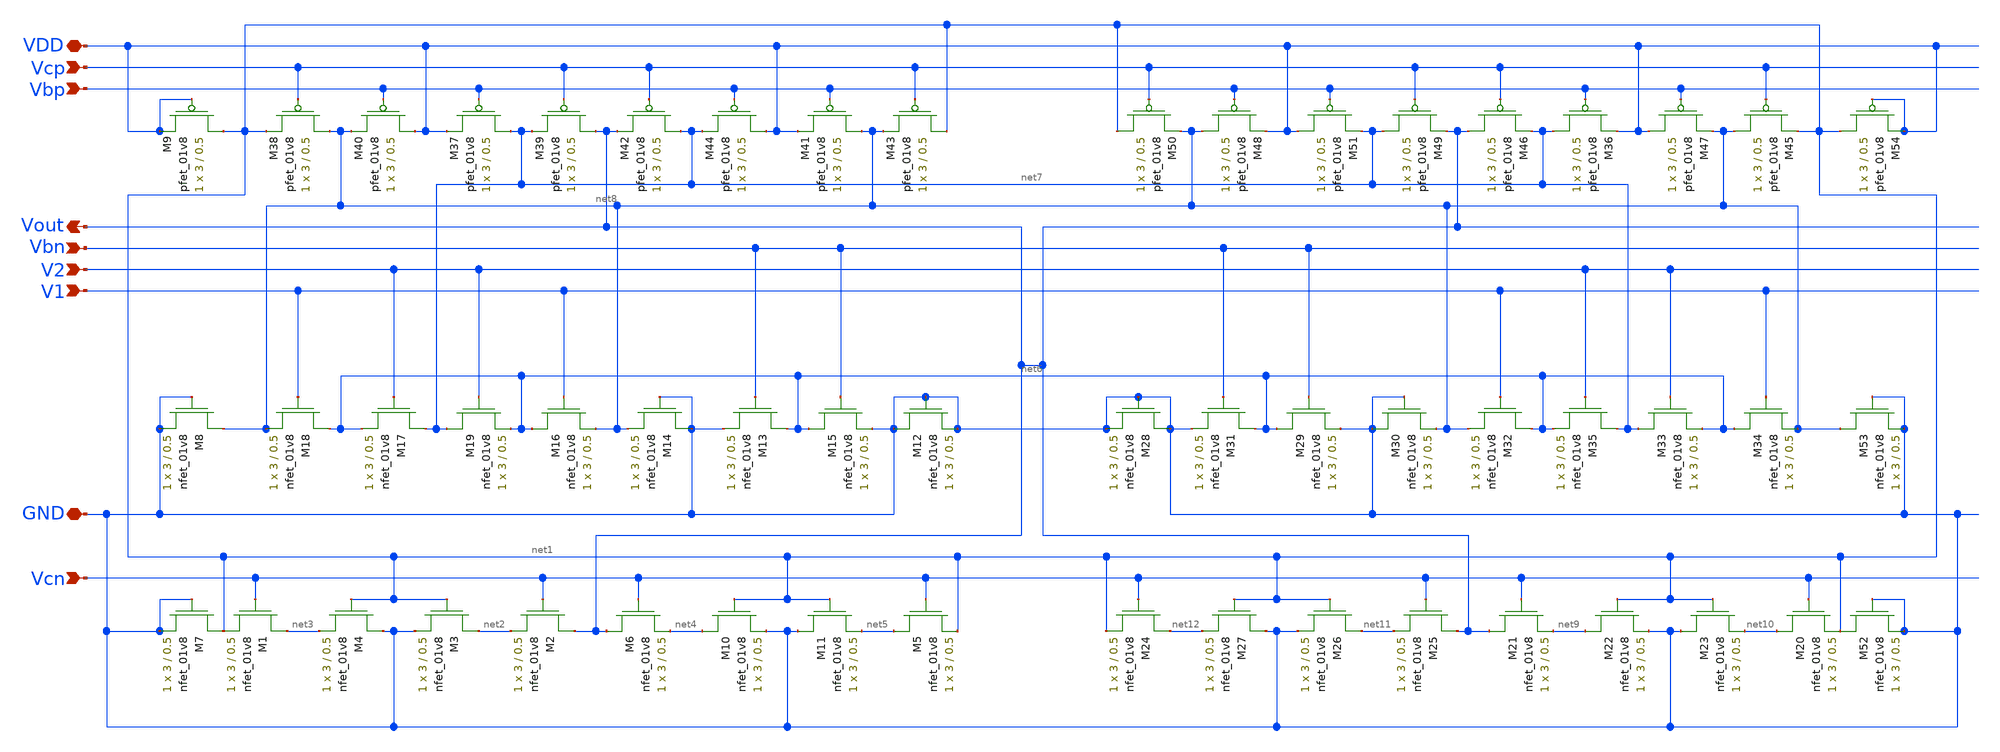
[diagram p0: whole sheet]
** sch_path: Miniproject3/layout&schematics/opamp.sch
**.subckt opamp Vcn Vout GND V1 V2 Vbn Vbp VDD Vcp
*.ipin Vcn
*.opin Vout
*.iopin GND
*.ipin V1
*.ipin V2
*.ipin Vbn
*.ipin Vbp
*.iopin VDD
*.ipin Vcp
XM1 net3 Vcn net1 GND sky130_fd_pr__nfet_01v8 L=0.5 W=3 nf=1 ad='int((nf+1)/2) * W/nf * 0.29' as='int((nf+2)/2) * W/nf * 0.29'
+ pd='2*int((nf+1)/2) * (W/nf + 0.29)' ps='2*int((nf+2)/2) * (W/nf + 0.29)' nrd='0.29 / W' nrs='0.29 / W'
+ sa=0 sb=0 sd=0 mult=1 m=1
XM2 Vout Vcn net2 GND sky130_fd_pr__nfet_01v8 L=0.5 W=3 nf=1 ad='int((nf+1)/2) * W/nf * 0.29' as='int((nf+2)/2) * W/nf * 0.29'
+ pd='2*int((nf+1)/2) * (W/nf + 0.29)' ps='2*int((nf+2)/2) * (W/nf + 0.29)' nrd='0.29 / W' nrs='0.29 / W'
+ sa=0 sb=0 sd=0 mult=1 m=1
XM3 net2 net1 GND GND sky130_fd_pr__nfet_01v8 L=0.5 W=3 nf=1 ad='int((nf+1)/2) * W/nf * 0.29' as='int((nf+2)/2) * W/nf * 0.29'
+ pd='2*int((nf+1)/2) * (W/nf + 0.29)' ps='2*int((nf+2)/2) * (W/nf + 0.29)' nrd='0.29 / W' nrs='0.29 / W'
+ sa=0 sb=0 sd=0 mult=1 m=1
XM4 GND net1 net3 GND sky130_fd_pr__nfet_01v8 L=0.5 W=3 nf=1 ad='int((nf+1)/2) * W/nf * 0.29' as='int((nf+2)/2) * W/nf * 0.29'
+ pd='2*int((nf+1)/2) * (W/nf + 0.29)' ps='2*int((nf+2)/2) * (W/nf + 0.29)' nrd='0.29 / W' nrs='0.29 / W'
+ sa=0 sb=0 sd=0 mult=1 m=1
XM5 net5 Vcn net1 GND sky130_fd_pr__nfet_01v8 L=0.5 W=3 nf=1 ad='int((nf+1)/2) * W/nf * 0.29' as='int((nf+2)/2) * W/nf * 0.29'
+ pd='2*int((nf+1)/2) * (W/nf + 0.29)' ps='2*int((nf+2)/2) * (W/nf + 0.29)' nrd='0.29 / W' nrs='0.29 / W'
+ sa=0 sb=0 sd=0 mult=1 m=1
XM6 Vout Vcn net4 GND sky130_fd_pr__nfet_01v8 L=0.5 W=3 nf=1 ad='int((nf+1)/2) * W/nf * 0.29' as='int((nf+2)/2) * W/nf * 0.29'
+ pd='2*int((nf+1)/2) * (W/nf + 0.29)' ps='2*int((nf+2)/2) * (W/nf + 0.29)' nrd='0.29 / W' nrs='0.29 / W'
+ sa=0 sb=0 sd=0 mult=1 m=1
XM10 net4 net1 GND GND sky130_fd_pr__nfet_01v8 L=0.5 W=3 nf=1 ad='int((nf+1)/2) * W/nf * 0.29' as='int((nf+2)/2) * W/nf * 0.29'
+ pd='2*int((nf+1)/2) * (W/nf + 0.29)' ps='2*int((nf+2)/2) * (W/nf + 0.29)' nrd='0.29 / W' nrs='0.29 / W'
+ sa=0 sb=0 sd=0 mult=1 m=1
XM11 GND net1 net5 GND sky130_fd_pr__nfet_01v8 L=0.5 W=3 nf=1 ad='int((nf+1)/2) * W/nf * 0.29' as='int((nf+2)/2) * W/nf * 0.29'
+ pd='2*int((nf+1)/2) * (W/nf + 0.29)' ps='2*int((nf+2)/2) * (W/nf + 0.29)' nrd='0.29 / W' nrs='0.29 / W'
+ sa=0 sb=0 sd=0 mult=1 m=1
XM12 GND GND GND GND sky130_fd_pr__nfet_01v8 L=0.5 W=3 nf=1 ad='int((nf+1)/2) * W/nf * 0.29' as='int((nf+2)/2) * W/nf * 0.29'
+ pd='2*int((nf+1)/2) * (W/nf + 0.29)' ps='2*int((nf+2)/2) * (W/nf + 0.29)' nrd='0.29 / W' nrs='0.29 / W'
+ sa=0 sb=0 sd=0 mult=1 m=1
XM13 net6 Vbn GND GND sky130_fd_pr__nfet_01v8 L=0.5 W=3 nf=1 ad='int((nf+1)/2) * W/nf * 0.29' as='int((nf+2)/2) * W/nf * 0.29'
+ pd='2*int((nf+1)/2) * (W/nf + 0.29)' ps='2*int((nf+2)/2) * (W/nf + 0.29)' nrd='0.29 / W' nrs='0.29 / W'
+ sa=0 sb=0 sd=0 mult=1 m=1
XM14 GND GND net8 GND sky130_fd_pr__nfet_01v8 L=0.5 W=3 nf=1 ad='int((nf+1)/2) * W/nf * 0.29' as='int((nf+2)/2) * W/nf * 0.29'
+ pd='2*int((nf+1)/2) * (W/nf + 0.29)' ps='2*int((nf+2)/2) * (W/nf + 0.29)' nrd='0.29 / W' nrs='0.29 / W'
+ sa=0 sb=0 sd=0 mult=1 m=1
XM15 net6 Vbn GND GND sky130_fd_pr__nfet_01v8 L=0.5 W=3 nf=1 ad='int((nf+1)/2) * W/nf * 0.29' as='int((nf+2)/2) * W/nf * 0.29'
+ pd='2*int((nf+1)/2) * (W/nf + 0.29)' ps='2*int((nf+2)/2) * (W/nf + 0.29)' nrd='0.29 / W' nrs='0.29 / W'
+ sa=0 sb=0 sd=0 mult=1 m=1
XM16 net6 V1 net8 GND sky130_fd_pr__nfet_01v8 L=0.5 W=3 nf=1 ad='int((nf+1)/2) * W/nf * 0.29' as='int((nf+2)/2) * W/nf * 0.29'
+ pd='2*int((nf+1)/2) * (W/nf + 0.29)' ps='2*int((nf+2)/2) * (W/nf + 0.29)' nrd='0.29 / W' nrs='0.29 / W'
+ sa=0 sb=0 sd=0 mult=1 m=1
XM17 net7 V2 net6 GND sky130_fd_pr__nfet_01v8 L=0.5 W=3 nf=1 ad='int((nf+1)/2) * W/nf * 0.29' as='int((nf+2)/2) * W/nf * 0.29'
+ pd='2*int((nf+1)/2) * (W/nf + 0.29)' ps='2*int((nf+2)/2) * (W/nf + 0.29)' nrd='0.29 / W' nrs='0.29 / W'
+ sa=0 sb=0 sd=0 mult=1 m=1
XM18 net6 V1 net8 GND sky130_fd_pr__nfet_01v8 L=0.5 W=3 nf=1 ad='int((nf+1)/2) * W/nf * 0.29' as='int((nf+2)/2) * W/nf * 0.29'
+ pd='2*int((nf+1)/2) * (W/nf + 0.29)' ps='2*int((nf+2)/2) * (W/nf + 0.29)' nrd='0.29 / W' nrs='0.29 / W'
+ sa=0 sb=0 sd=0 mult=1 m=1
XM19 net7 V2 net6 GND sky130_fd_pr__nfet_01v8 L=0.5 W=3 nf=1 ad='int((nf+1)/2) * W/nf * 0.29' as='int((nf+2)/2) * W/nf * 0.29'
+ pd='2*int((nf+1)/2) * (W/nf + 0.29)' ps='2*int((nf+2)/2) * (W/nf + 0.29)' nrd='0.29 / W' nrs='0.29 / W'
+ sa=0 sb=0 sd=0 mult=1 m=1
XM37 net7 Vbp VDD VDD sky130_fd_pr__pfet_01v8 L=0.5 W=3 nf=1 ad='int((nf+1)/2) * W/nf * 0.29' as='int((nf+2)/2) * W/nf * 0.29'
+ pd='2*int((nf+1)/2) * (W/nf + 0.29)' ps='2*int((nf+2)/2) * (W/nf + 0.29)' nrd='0.29 / W' nrs='0.29 / W'
+ sa=0 sb=0 sd=0 mult=1 m=1
XM38 net8 Vcp net1 VDD sky130_fd_pr__pfet_01v8 L=0.5 W=3 nf=1 ad='int((nf+1)/2) * W/nf * 0.29' as='int((nf+2)/2) * W/nf * 0.29'
+ pd='2*int((nf+1)/2) * (W/nf + 0.29)' ps='2*int((nf+2)/2) * (W/nf + 0.29)' nrd='0.29 / W' nrs='0.29 / W'
+ sa=0 sb=0 sd=0 mult=1 m=1
XM39 Vout Vcp net7 VDD sky130_fd_pr__pfet_01v8 L=0.5 W=3 nf=1 ad='int((nf+1)/2) * W/nf * 0.29' as='int((nf+2)/2) * W/nf * 0.29'
+ pd='2*int((nf+1)/2) * (W/nf + 0.29)' ps='2*int((nf+2)/2) * (W/nf + 0.29)' nrd='0.29 / W' nrs='0.29 / W'
+ sa=0 sb=0 sd=0 mult=1 m=1
XM40 VDD Vbp net8 VDD sky130_fd_pr__pfet_01v8 L=0.5 W=3 nf=1 ad='int((nf+1)/2) * W/nf * 0.29' as='int((nf+2)/2) * W/nf * 0.29'
+ pd='2*int((nf+1)/2) * (W/nf + 0.29)' ps='2*int((nf+2)/2) * (W/nf + 0.29)' nrd='0.29 / W' nrs='0.29 / W'
+ sa=0 sb=0 sd=0 mult=1 m=1
XM41 net8 Vbp VDD VDD sky130_fd_pr__pfet_01v8 L=0.5 W=3 nf=1 ad='int((nf+1)/2) * W/nf * 0.29' as='int((nf+2)/2) * W/nf * 0.29'
+ pd='2*int((nf+1)/2) * (W/nf + 0.29)' ps='2*int((nf+2)/2) * (W/nf + 0.29)' nrd='0.29 / W' nrs='0.29 / W'
+ sa=0 sb=0 sd=0 mult=1 m=1
XM42 net7 Vcp Vout VDD sky130_fd_pr__pfet_01v8 L=0.5 W=3 nf=1 ad='int((nf+1)/2) * W/nf * 0.29' as='int((nf+2)/2) * W/nf * 0.29'
+ pd='2*int((nf+1)/2) * (W/nf + 0.29)' ps='2*int((nf+2)/2) * (W/nf + 0.29)' nrd='0.29 / W' nrs='0.29 / W'
+ sa=0 sb=0 sd=0 mult=1 m=1
XM43 net1 Vcp net8 VDD sky130_fd_pr__pfet_01v8 L=0.5 W=3 nf=1 ad='int((nf+1)/2) * W/nf * 0.29' as='int((nf+2)/2) * W/nf * 0.29'
+ pd='2*int((nf+1)/2) * (W/nf + 0.29)' ps='2*int((nf+2)/2) * (W/nf + 0.29)' nrd='0.29 / W' nrs='0.29 / W'
+ sa=0 sb=0 sd=0 mult=1 m=1
XM44 VDD Vbp net7 VDD sky130_fd_pr__pfet_01v8 L=0.5 W=3 nf=1 ad='int((nf+1)/2) * W/nf * 0.29' as='int((nf+2)/2) * W/nf * 0.29'
+ pd='2*int((nf+1)/2) * (W/nf + 0.29)' ps='2*int((nf+2)/2) * (W/nf + 0.29)' nrd='0.29 / W' nrs='0.29 / W'
+ sa=0 sb=0 sd=0 mult=1 m=1
XM7 net1 GND GND GND sky130_fd_pr__nfet_01v8 L=0.5 W=3 nf=1 ad='int((nf+1)/2) * W/nf * 0.29' as='int((nf+2)/2) * W/nf * 0.29'
+ pd='2*int((nf+1)/2) * (W/nf + 0.29)' ps='2*int((nf+2)/2) * (W/nf + 0.29)' nrd='0.29 / W' nrs='0.29 / W'
+ sa=0 sb=0 sd=0 mult=1 m=1
XM8 net8 GND GND GND sky130_fd_pr__nfet_01v8 L=0.5 W=3 nf=1 ad='int((nf+1)/2) * W/nf * 0.29' as='int((nf+2)/2) * W/nf * 0.29'
+ pd='2*int((nf+1)/2) * (W/nf + 0.29)' ps='2*int((nf+2)/2) * (W/nf + 0.29)' nrd='0.29 / W' nrs='0.29 / W'
+ sa=0 sb=0 sd=0 mult=1 m=1
XM9 net1 VDD VDD VDD sky130_fd_pr__pfet_01v8 L=0.5 W=3 nf=1 ad='int((nf+1)/2) * W/nf * 0.29' as='int((nf+2)/2) * W/nf * 0.29'
+ pd='2*int((nf+1)/2) * (W/nf + 0.29)' ps='2*int((nf+2)/2) * (W/nf + 0.29)' nrd='0.29 / W' nrs='0.29 / W'
+ sa=0 sb=0 sd=0 mult=1 m=1
XM20 net10 Vcn net1 GND sky130_fd_pr__nfet_01v8 L=0.5 W=3 nf=1 ad='int((nf+1)/2) * W/nf * 0.29' as='int((nf+2)/2) * W/nf * 0.29'
+ pd='2*int((nf+1)/2) * (W/nf + 0.29)' ps='2*int((nf+2)/2) * (W/nf + 0.29)' nrd='0.29 / W' nrs='0.29 / W'
+ sa=0 sb=0 sd=0 mult=1 m=1
XM21 Vout Vcn net9 GND sky130_fd_pr__nfet_01v8 L=0.5 W=3 nf=1 ad='int((nf+1)/2) * W/nf * 0.29' as='int((nf+2)/2) * W/nf * 0.29'
+ pd='2*int((nf+1)/2) * (W/nf + 0.29)' ps='2*int((nf+2)/2) * (W/nf + 0.29)' nrd='0.29 / W' nrs='0.29 / W'
+ sa=0 sb=0 sd=0 mult=1 m=1
XM22 net9 net1 GND GND sky130_fd_pr__nfet_01v8 L=0.5 W=3 nf=1 ad='int((nf+1)/2) * W/nf * 0.29' as='int((nf+2)/2) * W/nf * 0.29'
+ pd='2*int((nf+1)/2) * (W/nf + 0.29)' ps='2*int((nf+2)/2) * (W/nf + 0.29)' nrd='0.29 / W' nrs='0.29 / W'
+ sa=0 sb=0 sd=0 mult=1 m=1
XM23 GND net1 net10 GND sky130_fd_pr__nfet_01v8 L=0.5 W=3 nf=1 ad='int((nf+1)/2) * W/nf * 0.29' as='int((nf+2)/2) * W/nf * 0.29'
+ pd='2*int((nf+1)/2) * (W/nf + 0.29)' ps='2*int((nf+2)/2) * (W/nf + 0.29)' nrd='0.29 / W' nrs='0.29 / W'
+ sa=0 sb=0 sd=0 mult=1 m=1
XM24 net12 Vcn net1 GND sky130_fd_pr__nfet_01v8 L=0.5 W=3 nf=1 ad='int((nf+1)/2) * W/nf * 0.29' as='int((nf+2)/2) * W/nf * 0.29'
+ pd='2*int((nf+1)/2) * (W/nf + 0.29)' ps='2*int((nf+2)/2) * (W/nf + 0.29)' nrd='0.29 / W' nrs='0.29 / W'
+ sa=0 sb=0 sd=0 mult=1 m=1
XM25 Vout Vcn net11 GND sky130_fd_pr__nfet_01v8 L=0.5 W=3 nf=1 ad='int((nf+1)/2) * W/nf * 0.29' as='int((nf+2)/2) * W/nf * 0.29'
+ pd='2*int((nf+1)/2) * (W/nf + 0.29)' ps='2*int((nf+2)/2) * (W/nf + 0.29)' nrd='0.29 / W' nrs='0.29 / W'
+ sa=0 sb=0 sd=0 mult=1 m=1
XM26 net11 net1 GND GND sky130_fd_pr__nfet_01v8 L=0.5 W=3 nf=1 ad='int((nf+1)/2) * W/nf * 0.29' as='int((nf+2)/2) * W/nf * 0.29'
+ pd='2*int((nf+1)/2) * (W/nf + 0.29)' ps='2*int((nf+2)/2) * (W/nf + 0.29)' nrd='0.29 / W' nrs='0.29 / W'
+ sa=0 sb=0 sd=0 mult=1 m=1
XM27 GND net1 net12 GND sky130_fd_pr__nfet_01v8 L=0.5 W=3 nf=1 ad='int((nf+1)/2) * W/nf * 0.29' as='int((nf+2)/2) * W/nf * 0.29'
+ pd='2*int((nf+1)/2) * (W/nf + 0.29)' ps='2*int((nf+2)/2) * (W/nf + 0.29)' nrd='0.29 / W' nrs='0.29 / W'
+ sa=0 sb=0 sd=0 mult=1 m=1
XM28 GND GND GND GND sky130_fd_pr__nfet_01v8 L=0.5 W=3 nf=1 ad='int((nf+1)/2) * W/nf * 0.29' as='int((nf+2)/2) * W/nf * 0.29'
+ pd='2*int((nf+1)/2) * (W/nf + 0.29)' ps='2*int((nf+2)/2) * (W/nf + 0.29)' nrd='0.29 / W' nrs='0.29 / W'
+ sa=0 sb=0 sd=0 mult=1 m=1
XM29 net6 Vbn GND GND sky130_fd_pr__nfet_01v8 L=0.5 W=3 nf=1 ad='int((nf+1)/2) * W/nf * 0.29' as='int((nf+2)/2) * W/nf * 0.29'
+ pd='2*int((nf+1)/2) * (W/nf + 0.29)' ps='2*int((nf+2)/2) * (W/nf + 0.29)' nrd='0.29 / W' nrs='0.29 / W'
+ sa=0 sb=0 sd=0 mult=1 m=1
XM30 GND GND net8 GND sky130_fd_pr__nfet_01v8 L=0.5 W=3 nf=1 ad='int((nf+1)/2) * W/nf * 0.29' as='int((nf+2)/2) * W/nf * 0.29'
+ pd='2*int((nf+1)/2) * (W/nf + 0.29)' ps='2*int((nf+2)/2) * (W/nf + 0.29)' nrd='0.29 / W' nrs='0.29 / W'
+ sa=0 sb=0 sd=0 mult=1 m=1
XM31 net6 Vbn GND GND sky130_fd_pr__nfet_01v8 L=0.5 W=3 nf=1 ad='int((nf+1)/2) * W/nf * 0.29' as='int((nf+2)/2) * W/nf * 0.29'
+ pd='2*int((nf+1)/2) * (W/nf + 0.29)' ps='2*int((nf+2)/2) * (W/nf + 0.29)' nrd='0.29 / W' nrs='0.29 / W'
+ sa=0 sb=0 sd=0 mult=1 m=1
XM32 net6 V1 net8 GND sky130_fd_pr__nfet_01v8 L=0.5 W=3 nf=1 ad='int((nf+1)/2) * W/nf * 0.29' as='int((nf+2)/2) * W/nf * 0.29'
+ pd='2*int((nf+1)/2) * (W/nf + 0.29)' ps='2*int((nf+2)/2) * (W/nf + 0.29)' nrd='0.29 / W' nrs='0.29 / W'
+ sa=0 sb=0 sd=0 mult=1 m=1
XM33 net7 V2 net6 GND sky130_fd_pr__nfet_01v8 L=0.5 W=3 nf=1 ad='int((nf+1)/2) * W/nf * 0.29' as='int((nf+2)/2) * W/nf * 0.29'
+ pd='2*int((nf+1)/2) * (W/nf + 0.29)' ps='2*int((nf+2)/2) * (W/nf + 0.29)' nrd='0.29 / W' nrs='0.29 / W'
+ sa=0 sb=0 sd=0 mult=1 m=1
XM34 net6 V1 net8 GND sky130_fd_pr__nfet_01v8 L=0.5 W=3 nf=1 ad='int((nf+1)/2) * W/nf * 0.29' as='int((nf+2)/2) * W/nf * 0.29'
+ pd='2*int((nf+1)/2) * (W/nf + 0.29)' ps='2*int((nf+2)/2) * (W/nf + 0.29)' nrd='0.29 / W' nrs='0.29 / W'
+ sa=0 sb=0 sd=0 mult=1 m=1
XM35 net7 V2 net6 GND sky130_fd_pr__nfet_01v8 L=0.5 W=3 nf=1 ad='int((nf+1)/2) * W/nf * 0.29' as='int((nf+2)/2) * W/nf * 0.29'
+ pd='2*int((nf+1)/2) * (W/nf + 0.29)' ps='2*int((nf+2)/2) * (W/nf + 0.29)' nrd='0.29 / W' nrs='0.29 / W'
+ sa=0 sb=0 sd=0 mult=1 m=1
XM36 net7 Vbp VDD VDD sky130_fd_pr__pfet_01v8 L=0.5 W=3 nf=1 ad='int((nf+1)/2) * W/nf * 0.29' as='int((nf+2)/2) * W/nf * 0.29'
+ pd='2*int((nf+1)/2) * (W/nf + 0.29)' ps='2*int((nf+2)/2) * (W/nf + 0.29)' nrd='0.29 / W' nrs='0.29 / W'
+ sa=0 sb=0 sd=0 mult=1 m=1
XM45 net8 Vcp net1 VDD sky130_fd_pr__pfet_01v8 L=0.5 W=3 nf=1 ad='int((nf+1)/2) * W/nf * 0.29' as='int((nf+2)/2) * W/nf * 0.29'
+ pd='2*int((nf+1)/2) * (W/nf + 0.29)' ps='2*int((nf+2)/2) * (W/nf + 0.29)' nrd='0.29 / W' nrs='0.29 / W'
+ sa=0 sb=0 sd=0 mult=1 m=1
XM46 Vout Vcp net7 VDD sky130_fd_pr__pfet_01v8 L=0.5 W=3 nf=1 ad='int((nf+1)/2) * W/nf * 0.29' as='int((nf+2)/2) * W/nf * 0.29'
+ pd='2*int((nf+1)/2) * (W/nf + 0.29)' ps='2*int((nf+2)/2) * (W/nf + 0.29)' nrd='0.29 / W' nrs='0.29 / W'
+ sa=0 sb=0 sd=0 mult=1 m=1
XM47 VDD Vbp net8 VDD sky130_fd_pr__pfet_01v8 L=0.5 W=3 nf=1 ad='int((nf+1)/2) * W/nf * 0.29' as='int((nf+2)/2) * W/nf * 0.29'
+ pd='2*int((nf+1)/2) * (W/nf + 0.29)' ps='2*int((nf+2)/2) * (W/nf + 0.29)' nrd='0.29 / W' nrs='0.29 / W'
+ sa=0 sb=0 sd=0 mult=1 m=1
XM48 net8 Vbp VDD VDD sky130_fd_pr__pfet_01v8 L=0.5 W=3 nf=1 ad='int((nf+1)/2) * W/nf * 0.29' as='int((nf+2)/2) * W/nf * 0.29'
+ pd='2*int((nf+1)/2) * (W/nf + 0.29)' ps='2*int((nf+2)/2) * (W/nf + 0.29)' nrd='0.29 / W' nrs='0.29 / W'
+ sa=0 sb=0 sd=0 mult=1 m=1
XM49 net7 Vcp Vout VDD sky130_fd_pr__pfet_01v8 L=0.5 W=3 nf=1 ad='int((nf+1)/2) * W/nf * 0.29' as='int((nf+2)/2) * W/nf * 0.29'
+ pd='2*int((nf+1)/2) * (W/nf + 0.29)' ps='2*int((nf+2)/2) * (W/nf + 0.29)' nrd='0.29 / W' nrs='0.29 / W'
+ sa=0 sb=0 sd=0 mult=1 m=1
XM50 net1 Vcp net8 VDD sky130_fd_pr__pfet_01v8 L=0.5 W=3 nf=1 ad='int((nf+1)/2) * W/nf * 0.29' as='int((nf+2)/2) * W/nf * 0.29'
+ pd='2*int((nf+1)/2) * (W/nf + 0.29)' ps='2*int((nf+2)/2) * (W/nf + 0.29)' nrd='0.29 / W' nrs='0.29 / W'
+ sa=0 sb=0 sd=0 mult=1 m=1
XM51 VDD Vbp net7 VDD sky130_fd_pr__pfet_01v8 L=0.5 W=3 nf=1 ad='int((nf+1)/2) * W/nf * 0.29' as='int((nf+2)/2) * W/nf * 0.29'
+ pd='2*int((nf+1)/2) * (W/nf + 0.29)' ps='2*int((nf+2)/2) * (W/nf + 0.29)' nrd='0.29 / W' nrs='0.29 / W'
+ sa=0 sb=0 sd=0 mult=1 m=1
XM52 net1 GND GND GND sky130_fd_pr__nfet_01v8 L=0.5 W=3 nf=1 ad='int((nf+1)/2) * W/nf * 0.29' as='int((nf+2)/2) * W/nf * 0.29'
+ pd='2*int((nf+1)/2) * (W/nf + 0.29)' ps='2*int((nf+2)/2) * (W/nf + 0.29)' nrd='0.29 / W' nrs='0.29 / W'
+ sa=0 sb=0 sd=0 mult=1 m=1
XM53 net8 GND GND GND sky130_fd_pr__nfet_01v8 L=0.5 W=3 nf=1 ad='int((nf+1)/2) * W/nf * 0.29' as='int((nf+2)/2) * W/nf * 0.29'
+ pd='2*int((nf+1)/2) * (W/nf + 0.29)' ps='2*int((nf+2)/2) * (W/nf + 0.29)' nrd='0.29 / W' nrs='0.29 / W'
+ sa=0 sb=0 sd=0 mult=1 m=1
XM54 net1 VDD VDD VDD sky130_fd_pr__pfet_01v8 L=0.5 W=3 nf=1 ad='int((nf+1)/2) * W/nf * 0.29' as='int((nf+2)/2) * W/nf * 0.29'
+ pd='2*int((nf+1)/2) * (W/nf + 0.29)' ps='2*int((nf+2)/2) * (W/nf + 0.29)' nrd='0.29 / W' nrs='0.29 / W'
+ sa=0 sb=0 sd=0 mult=1 m=1
**.ends
.end
